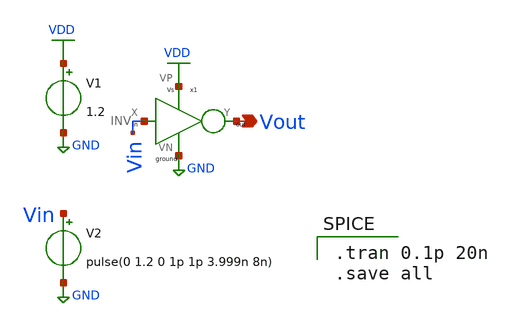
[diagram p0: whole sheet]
** sch_path: component/INV/INV_sym_test.sch
**.subckt INV_sym_test Vout
*.opin Vout
V1 VDD GND 1.2
V2 Vin GND pulse(0 1.2 0 1p 1p 3.999n 8n)
x1 Vin Vout VDD GND INV
**** begin user architecture code

** opencircuitdesign pdks install
.lib $::SKYWATER_MODELS/sky130.lib.spice tt



.tran 0.1p 20n
.save all

**** end user architecture code
**.ends

* expanding   symbol:  Pico_project/INV/INV.sym # of pins=4
** sym_path: component/INV/INV.sym
** sch_path: component/INV/INV.sch
.subckt INV X Y VP VN
*.ipin X
*.opin Y
*.iopin VN
*.iopin VP
XM1 Y X VN VN sky130_fd_pr__nfet_01v8 L=0.15 W=0.42 nf=1 ad='int((nf+1)/2) * W/nf * 0.29' as='int((nf+2)/2) * W/nf * 0.29'
+ pd='2*int((nf+1)/2) * (W/nf + 0.29)' ps='2*int((nf+2)/2) * (W/nf + 0.29)' nrd='0.29 / W' nrs='0.29 / W'
+ sa=0 sb=0 sd=0 mult=1 m=1
XM2 Y X VP VP sky130_fd_pr__pfet_01v8 L=0.15 W=1.26 nf=1 ad='int((nf+1)/2) * W/nf * 0.29' as='int((nf+2)/2) * W/nf * 0.29'
+ pd='2*int((nf+1)/2) * (W/nf + 0.29)' ps='2*int((nf+2)/2) * (W/nf + 0.29)' nrd='0.29 / W' nrs='0.29 / W'
+ sa=0 sb=0 sd=0 mult=1 m=1
.ends

.GLOBAL GND
.GLOBAL VDD
.end
